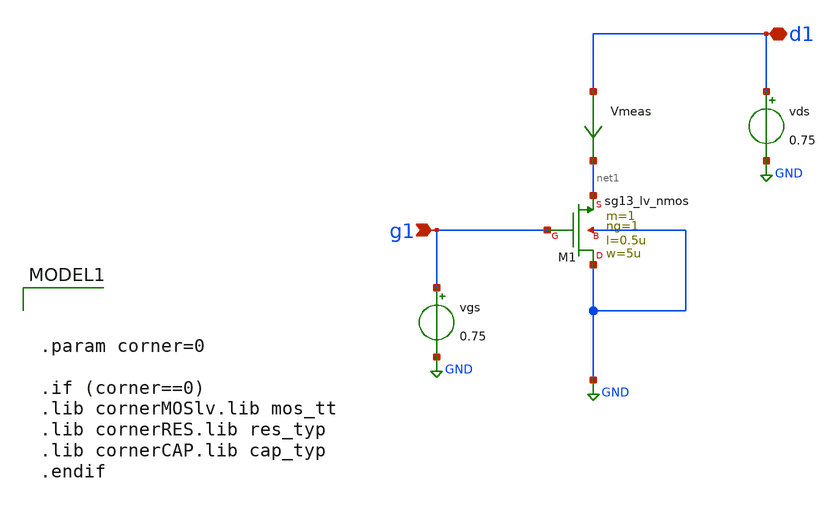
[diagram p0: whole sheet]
** sch_path: Tarea1/lv_mos_characterization.sch
**.subckt lv_mos_characterization g1 d1
*.ipin g1
*.iopin d1
XM1 GND g1 net1 GND sg13_lv_nmos w=5u l=0.5u ng=1 m=1 mm_ok=1
Vmeas d1 net1 0
.save i(vmeas)
vgs g1 GND 0.75
vds d1 GND 0.75
**** begin user architecture code


.param corner=0

.if (corner==0)
.lib cornerMOSlv.lib mos_tt
.lib cornerRES.lib res_typ
.lib cornerCAP.lib cap_typ
.endif



.control
save all
save @n.xm1.nsg13_lv_nmos[ids]
save @n.xm1.nsg13_lv_nmos[gm]
op

dc vgs 0.01 1.8 0.01 vds 0.45 1.35 0.45

let idn = @n.xm1.nsg13_lv_nmos[ids]
let gmn = @n.xm1.nsg13_lv_nmos[gm]
let vthn = @n.xm1.nsg13_lv_nmos[vth]
let vgsn = @n.xm1.nsg13_lv_nmos[vgs]
let vdsatn = @n.xm1.nsg13_lv_nmos[vdss]
let cgg = @n.xm1.nsg13_lv_nmos[cgg]
let cgsol = @n.xm1.nsg13_lv_nmos[cgsol]
let cgdol = @n.xm1.nsg13_lv_nmos[cgdol]
let vov = 2*idn/gmn
let gmoverId = gmn/idn
let cgg_tot = cgg + cgsol + cgdol
let ft = 1e-9*gmn/6.28/cgg_tot

plot i(Vmeas)
*plot ylog i(Vmeas)
*plot gmn
*plot xlog gmoverId

wrdata data_nmos_idvgs_VDSp9_test.txt idn

wrdata data_nmos_idvgs_VDSp9_gmid-ft.txt gmoverId ft

**Pregunta B
reset
dc vds 0 1.35 0.01  vgs 0.4 0.8 0.4
plot i(Vmeas)
reset
dc vds 0 1.35 0.01 vgs 1.5 1.5 0.01
plot i(Vmeas)

**Pregunta C
reset

save all
save @n.xm1.nsg13_lv_nmos[gm]
dc vgs 0 1.5 0.01

let gmn2 = @n.xm1.nsg13_lv_nmos[gm]
let ft = gmn2/(2*pi*@n.xm1.nsg13_lv_nmos[cgg])
plot gmn2/i(Vmeas)
plot ft

.endc


**** end user architecture code
**.ends
.GLOBAL GND
.end
